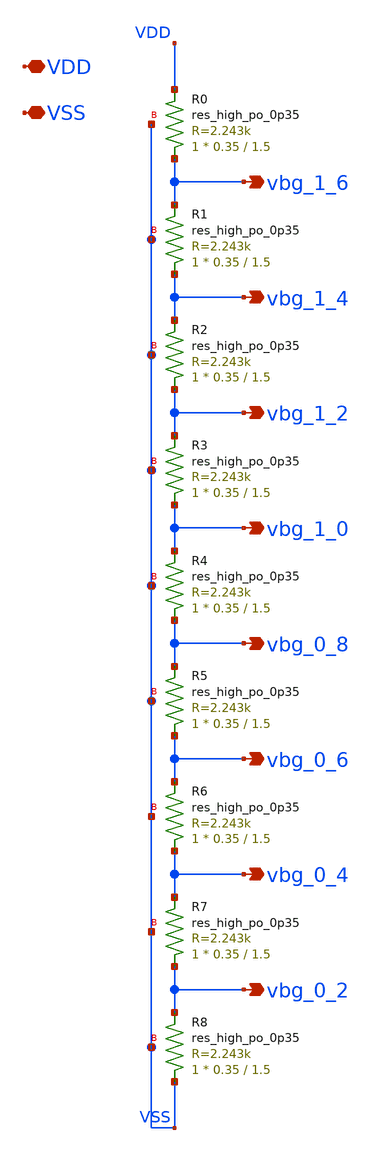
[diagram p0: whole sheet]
** sch_path: xschem/BG.sch
**.subckt BG vbg_1_6 vbg_1_4 vbg_1_2 vbg_1_0 vbg_0_8 vbg_0_6 vbg_0_4 vbg_0_2 VDD VSS
*.opin vbg_1_6
*.opin vbg_1_4
*.opin vbg_1_2
*.opin vbg_1_0
*.opin vbg_0_8
*.opin vbg_0_6
*.opin vbg_0_4
*.opin vbg_0_2
*.iopin VDD
*.iopin VSS
XR1 vbg_1_4 vbg_1_6 VSS sky130_fd_pr__res_high_po_0p35 L=1.5 mult=1 m=1
XR0 vbg_1_6 VDD VSS sky130_fd_pr__res_high_po_0p35 L=1.5 mult=1 m=1
XR3 vbg_1_0 vbg_1_2 VSS sky130_fd_pr__res_high_po_0p35 L=1.5 mult=1 m=1
XR2 vbg_1_2 vbg_1_4 VSS sky130_fd_pr__res_high_po_0p35 L=1.5 mult=1 m=1
XR5 vbg_0_6 vbg_0_8 VSS sky130_fd_pr__res_high_po_0p35 L=1.5 mult=1 m=1
XR4 vbg_0_8 vbg_1_0 VSS sky130_fd_pr__res_high_po_0p35 L=1.5 mult=1 m=1
XR6 vbg_0_4 vbg_0_6 VSS sky130_fd_pr__res_high_po_0p35 L=1.5 mult=1 m=1
XR7 vbg_0_2 vbg_0_4 VSS sky130_fd_pr__res_high_po_0p35 L=1.5 mult=1 m=1
XR8 VSS vbg_0_2 VSS sky130_fd_pr__res_high_po_0p35 L=1.5 mult=1 m=1
**.ends
.end
